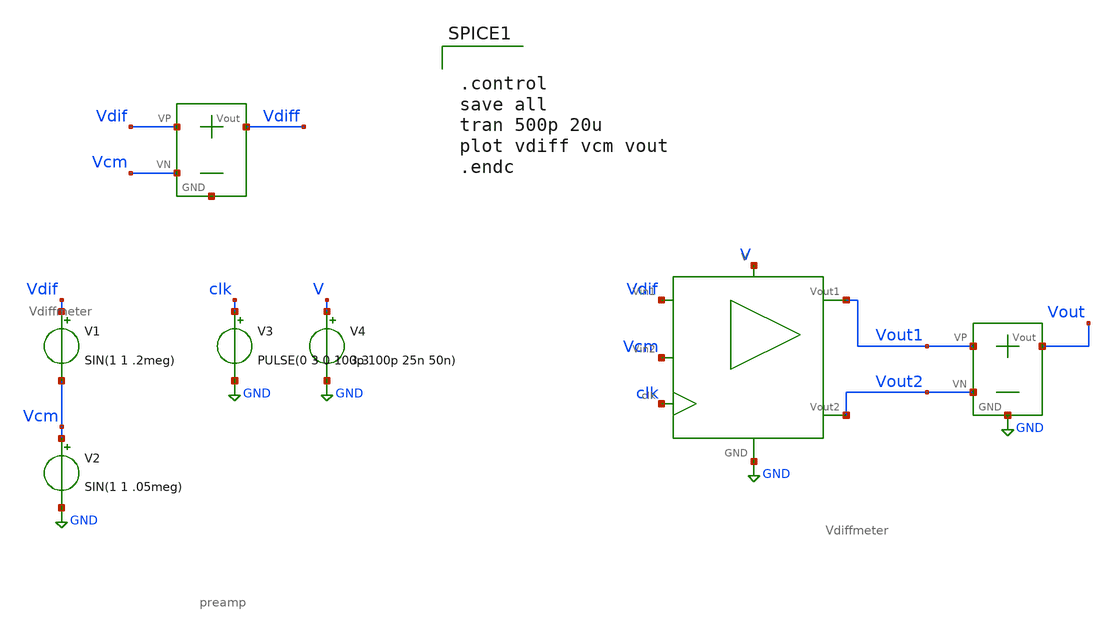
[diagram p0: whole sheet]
** sch_path: SAR_ADC/xschem/test/preamp_tb/sin_100k-sin_200k__tb.sch
**.subckt sin_100k-sin_200k__tb
V1 Vdif Vcm SIN(1 1 .2meg)
V2 Vcm GND SIN(1 1 .05meg)
V3 clk GND PULSE(0 3 0 100p 100p 25n 50n)
V4 V GND 3.3
X1 V GND Vdif clk Vout1 Vout2 Vcm preamp
X3 Vout1 Vout2 Vout GND Vdiffmeter
X2 Vdif Vcm Vdiff net1 Vdiffmeter
**** begin user architecture code


.control
save all
tran 500p 20u
plot vdiff vcm vout
.endc


.include /foss/pdks/gf180mcuC/libs.tech/ngspice/design.ngspice
.lib /foss/pdks/gf180mcuC/libs.tech/ngspice/sm141064.ngspice typical

**** end user architecture code
**.ends
.GLOBAL GND
.end
